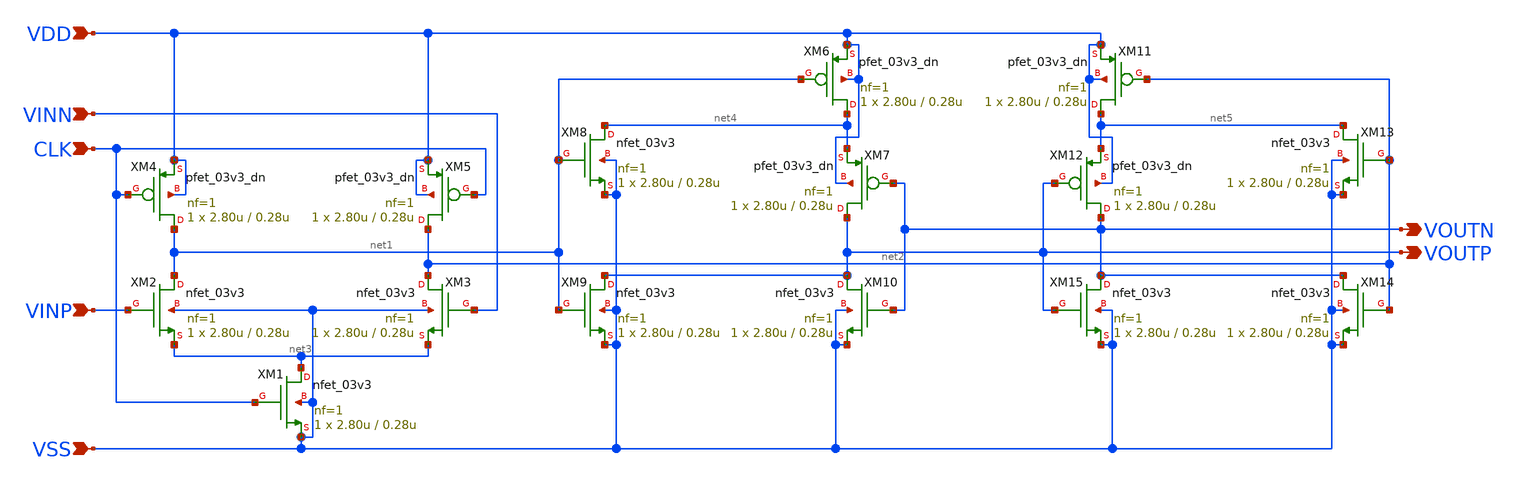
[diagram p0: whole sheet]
** sch_path: gitefu/comp_20240331/comp_20240331.sch
**.subckt comp_20240331 VDD CLK VINP VINN VSS VOUTP VOUTN
*.ipin VDD
*.ipin CLK
*.ipin VINP
*.ipin VINN
*.ipin VSS
*.opin VOUTP
*.opin VOUTN
XM1 net3 CLK VSS VSS nfet_03v3 L=0.28u W=2.80u nf=1 ad='int((nf+1)/2) * W/nf * 0.18u' as='int((nf+2)/2) * W/nf * 0.18u'
+ pd='2*int((nf+1)/2) * (W/nf + 0.18u)' ps='2*int((nf+2)/2) * (W/nf + 0.18u)' nrd='0.18u / W' nrs='0.18u / W'
+ sa=0 sb=0 sd=0 m=1
XM2 net1 VINP net3 VSS nfet_03v3 L=0.28u W=2.80u nf=1 ad='int((nf+1)/2) * W/nf * 0.18u' as='int((nf+2)/2) * W/nf * 0.18u'
+ pd='2*int((nf+1)/2) * (W/nf + 0.18u)' ps='2*int((nf+2)/2) * (W/nf + 0.18u)' nrd='0.18u / W' nrs='0.18u / W'
+ sa=0 sb=0 sd=0 m=1
XM4 net1 CLK VDD VDD pfet_03v3_dn L=0.28u W=2.80u nf=1 ad='int((nf+1)/2) * W/nf * 0.18u' as='int((nf+2)/2) * W/nf * 0.18u'
+ pd='2*int((nf+1)/2) * (W/nf + 0.18u)' ps='2*int((nf+2)/2) * (W/nf + 0.18u)' nrd='0.18u / W' nrs='0.18u / W'
+ sa=0 sb=0 sd=0 m=1
XM6 net4 net1 VDD VDD pfet_03v3_dn L=0.28u W=2.80u nf=1 ad='int((nf+1)/2) * W/nf * 0.18u' as='int((nf+2)/2) * W/nf * 0.18u'
+ pd='2*int((nf+1)/2) * (W/nf + 0.18u)' ps='2*int((nf+2)/2) * (W/nf + 0.18u)' nrd='0.18u / W' nrs='0.18u / W'
+ sa=0 sb=0 sd=0 m=1
XM7 VOUTP VOUTN net4 VDD pfet_03v3_dn L=0.28u W=2.80u nf=1 ad='int((nf+1)/2) * W/nf * 0.18u' as='int((nf+2)/2) * W/nf * 0.18u'
+ pd='2*int((nf+1)/2) * (W/nf + 0.18u)' ps='2*int((nf+2)/2) * (W/nf + 0.18u)' nrd='0.18u / W' nrs='0.18u / W'
+ sa=0 sb=0 sd=0 m=1
XM8 net4 net1 VSS VSS nfet_03v3 L=0.28u W=2.80u nf=1 ad='int((nf+1)/2) * W/nf * 0.18u' as='int((nf+2)/2) * W/nf * 0.18u'
+ pd='2*int((nf+1)/2) * (W/nf + 0.18u)' ps='2*int((nf+2)/2) * (W/nf + 0.18u)' nrd='0.18u / W' nrs='0.18u / W'
+ sa=0 sb=0 sd=0 m=1
XM9 VOUTP net1 VSS VSS nfet_03v3 L=0.28u W=2.80u nf=1 ad='int((nf+1)/2) * W/nf * 0.18u' as='int((nf+2)/2) * W/nf * 0.18u'
+ pd='2*int((nf+1)/2) * (W/nf + 0.18u)' ps='2*int((nf+2)/2) * (W/nf + 0.18u)' nrd='0.18u / W' nrs='0.18u / W'
+ sa=0 sb=0 sd=0 m=1
XM10 VOUTP VOUTN VSS VSS nfet_03v3 L=0.28u W=2.80u nf=1 ad='int((nf+1)/2) * W/nf * 0.18u' as='int((nf+2)/2) * W/nf * 0.18u'
+ pd='2*int((nf+1)/2) * (W/nf + 0.18u)' ps='2*int((nf+2)/2) * (W/nf + 0.18u)' nrd='0.18u / W' nrs='0.18u / W'
+ sa=0 sb=0 sd=0 m=1
XM3 net2 VINN net3 VSS nfet_03v3 L=0.28u W=2.80u nf=1 ad='int((nf+1)/2) * W/nf * 0.18u' as='int((nf+2)/2) * W/nf * 0.18u'
+ pd='2*int((nf+1)/2) * (W/nf + 0.18u)' ps='2*int((nf+2)/2) * (W/nf + 0.18u)' nrd='0.18u / W' nrs='0.18u / W'
+ sa=0 sb=0 sd=0 m=1
XM5 net2 CLK VDD VDD pfet_03v3_dn L=0.28u W=2.80u nf=1 ad='int((nf+1)/2) * W/nf * 0.18u' as='int((nf+2)/2) * W/nf * 0.18u'
+ pd='2*int((nf+1)/2) * (W/nf + 0.18u)' ps='2*int((nf+2)/2) * (W/nf + 0.18u)' nrd='0.18u / W' nrs='0.18u / W'
+ sa=0 sb=0 sd=0 m=1
XM11 net5 net2 VDD VDD pfet_03v3_dn L=0.28u W=2.80u nf=1 ad='int((nf+1)/2) * W/nf * 0.18u' as='int((nf+2)/2) * W/nf * 0.18u'
+ pd='2*int((nf+1)/2) * (W/nf + 0.18u)' ps='2*int((nf+2)/2) * (W/nf + 0.18u)' nrd='0.18u / W' nrs='0.18u / W'
+ sa=0 sb=0 sd=0 m=1
XM12 VOUTN VOUTP net5 VDD pfet_03v3_dn L=0.28u W=2.80u nf=1 ad='int((nf+1)/2) * W/nf * 0.18u' as='int((nf+2)/2) * W/nf * 0.18u'
+ pd='2*int((nf+1)/2) * (W/nf + 0.18u)' ps='2*int((nf+2)/2) * (W/nf + 0.18u)' nrd='0.18u / W' nrs='0.18u / W'
+ sa=0 sb=0 sd=0 m=1
XM13 net5 net2 VSS VSS nfet_03v3 L=0.28u W=2.80u nf=1 ad='int((nf+1)/2) * W/nf * 0.18u' as='int((nf+2)/2) * W/nf * 0.18u'
+ pd='2*int((nf+1)/2) * (W/nf + 0.18u)' ps='2*int((nf+2)/2) * (W/nf + 0.18u)' nrd='0.18u / W' nrs='0.18u / W'
+ sa=0 sb=0 sd=0 m=1
XM14 VOUTN net2 VSS VSS nfet_03v3 L=0.28u W=2.80u nf=1 ad='int((nf+1)/2) * W/nf * 0.18u' as='int((nf+2)/2) * W/nf * 0.18u'
+ pd='2*int((nf+1)/2) * (W/nf + 0.18u)' ps='2*int((nf+2)/2) * (W/nf + 0.18u)' nrd='0.18u / W' nrs='0.18u / W'
+ sa=0 sb=0 sd=0 m=1
XM15 VOUTN VOUTP VSS VSS nfet_03v3 L=0.28u W=2.80u nf=1 ad='int((nf+1)/2) * W/nf * 0.18u' as='int((nf+2)/2) * W/nf * 0.18u'
+ pd='2*int((nf+1)/2) * (W/nf + 0.18u)' ps='2*int((nf+2)/2) * (W/nf + 0.18u)' nrd='0.18u / W' nrs='0.18u / W'
+ sa=0 sb=0 sd=0 m=1
**.ends
.end
